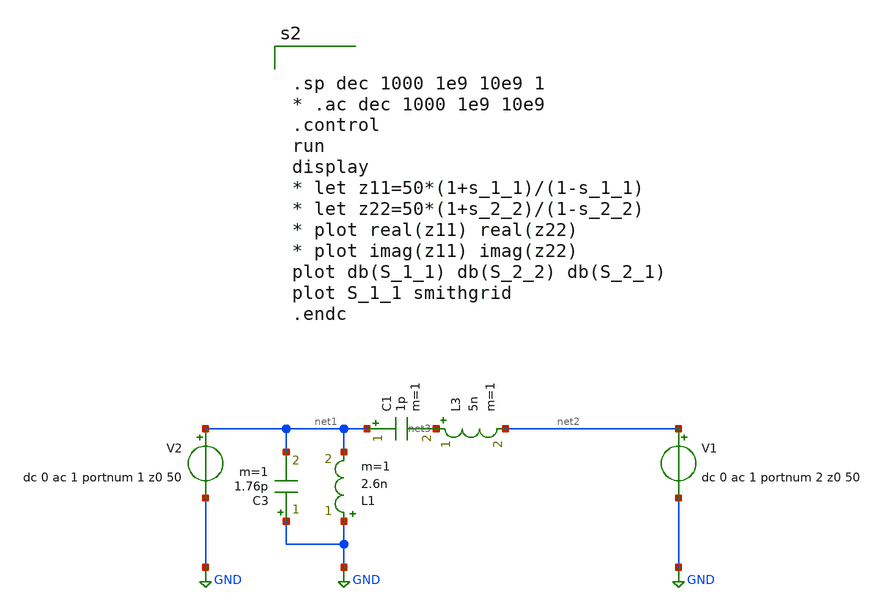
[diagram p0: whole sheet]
** sch_path: xschem/sptest.sch
**.subckt sptest
V2 net1 GND dc 0 ac 1 portnum 1 z0 50
V1 net2 GND dc 0 ac 1 portnum 2 z0 50
L3 net3 net2 5n m=1
C3 GND net1 1.76p m=1
L1 GND net1 2.6n m=1
C1 net1 net3 1p m=1
**** begin user architecture code


.sp dec 1000 1e9 10e9 1
* .ac dec 1000 1e9 10e9
.control
run
display
* let z11=50*(1+s_1_1)/(1-s_1_1)
* let z22=50*(1+s_2_2)/(1-s_2_2)
* plot real(z11) real(z22)
* plot imag(z11) imag(z22)
plot db(S_1_1) db(S_2_2) db(S_2_1)
plot S_1_1 smithgrid
.endc


**** end user architecture code
**.ends
.GLOBAL GND
.end
